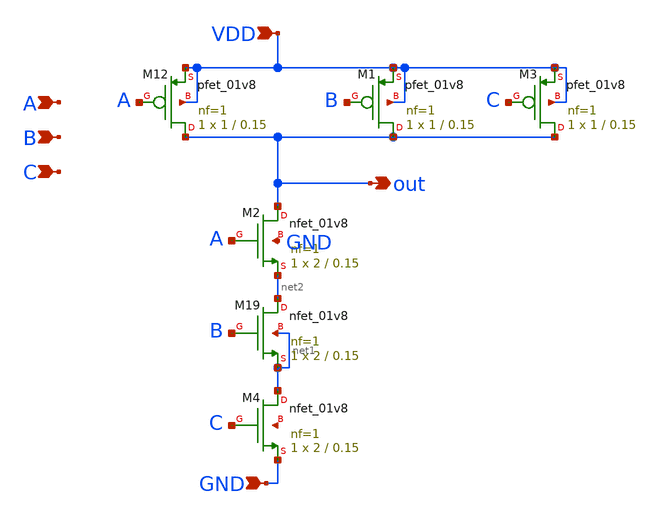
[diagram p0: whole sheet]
** sch_path: xschem/untitled-2.sch
**.subckt untitled-2 VDD GND out A B C
*.ipin VDD
*.ipin GND
*.opin out
*.ipin A
*.ipin B
*.ipin C
XM12 out A VDD VDD sky130_fd_pr__pfet_01v8 L=0.15 W=1 nf=1 ad='int((nf+1)/2) * W/nf * 0.29' as='int((nf+2)/2) * W/nf * 0.29'
+ pd='2*int((nf+1)/2) * (W/nf + 0.29)' ps='2*int((nf+2)/2) * (W/nf + 0.29)' nrd='0.29 / W' nrs='0.29 / W'
+ sa=0 sb=0 sd=0 mult=1 m=1
XM19 net2 B net1 net1 sky130_fd_pr__nfet_01v8 L=0.15 W=2 nf=1 ad='int((nf+1)/2) * W/nf * 0.29' as='int((nf+2)/2) * W/nf * 0.29'
+ pd='2*int((nf+1)/2) * (W/nf + 0.29)' ps='2*int((nf+2)/2) * (W/nf + 0.29)' nrd='0.29 / W' nrs='0.29 / W'
+ sa=0 sb=0 sd=0 mult=1 m=1
XM1 out B VDD VDD sky130_fd_pr__pfet_01v8 L=0.15 W=1 nf=1 ad='int((nf+1)/2) * W/nf * 0.29' as='int((nf+2)/2) * W/nf * 0.29'
+ pd='2*int((nf+1)/2) * (W/nf + 0.29)' ps='2*int((nf+2)/2) * (W/nf + 0.29)' nrd='0.29 / W' nrs='0.29 / W'
+ sa=0 sb=0 sd=0 mult=1 m=1
XM2 out A net2 GND sky130_fd_pr__nfet_01v8 L=0.15 W=2 nf=1 ad='int((nf+1)/2) * W/nf * 0.29' as='int((nf+2)/2) * W/nf * 0.29'
+ pd='2*int((nf+1)/2) * (W/nf + 0.29)' ps='2*int((nf+2)/2) * (W/nf + 0.29)' nrd='0.29 / W' nrs='0.29 / W'
+ sa=0 sb=0 sd=0 mult=1 m=1
XM3 out C VDD VDD sky130_fd_pr__pfet_01v8 L=0.15 W=1 nf=1 ad='int((nf+1)/2) * W/nf * 0.29' as='int((nf+2)/2) * W/nf * 0.29'
+ pd='2*int((nf+1)/2) * (W/nf + 0.29)' ps='2*int((nf+2)/2) * (W/nf + 0.29)' nrd='0.29 / W' nrs='0.29 / W'
+ sa=0 sb=0 sd=0 mult=1 m=1
XM4 net1 C GND net3 sky130_fd_pr__nfet_01v8 L=0.15 W=2 nf=1 ad='int((nf+1)/2) * W/nf * 0.29' as='int((nf+2)/2) * W/nf * 0.29'
+ pd='2*int((nf+1)/2) * (W/nf + 0.29)' ps='2*int((nf+2)/2) * (W/nf + 0.29)' nrd='0.29 / W' nrs='0.29 / W'
+ sa=0 sb=0 sd=0 mult=1 m=1
**.ends
.end
